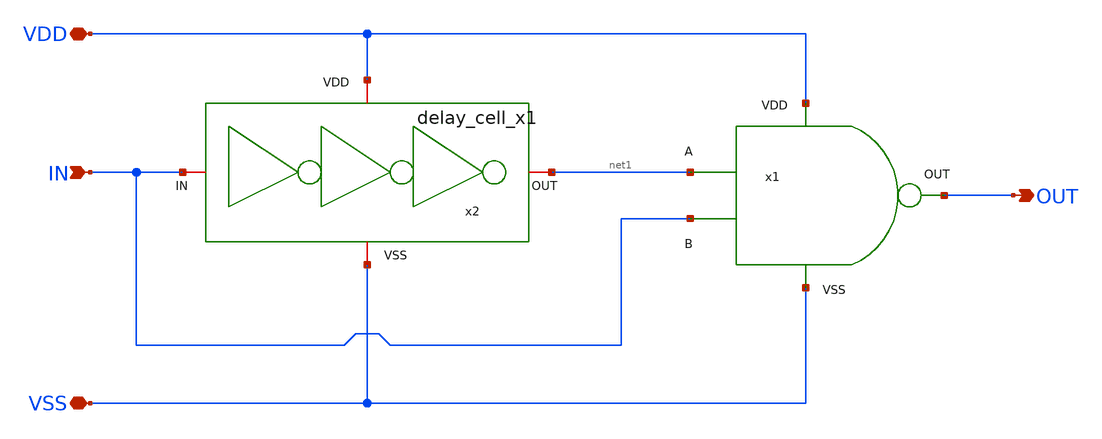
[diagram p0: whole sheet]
** sch_path: designs/sar_adc/digital/edge_detector/xschem/edge_detector.sch
**.subckt edge_detector VDD VSS IN OUT
*.iopin VDD
*.iopin VSS
*.ipin IN
*.opin OUT
x1 VDD VSS net1 IN OUT NAND
x2 VDD IN net1 VSS delay_cell_x1
**.ends
.end
